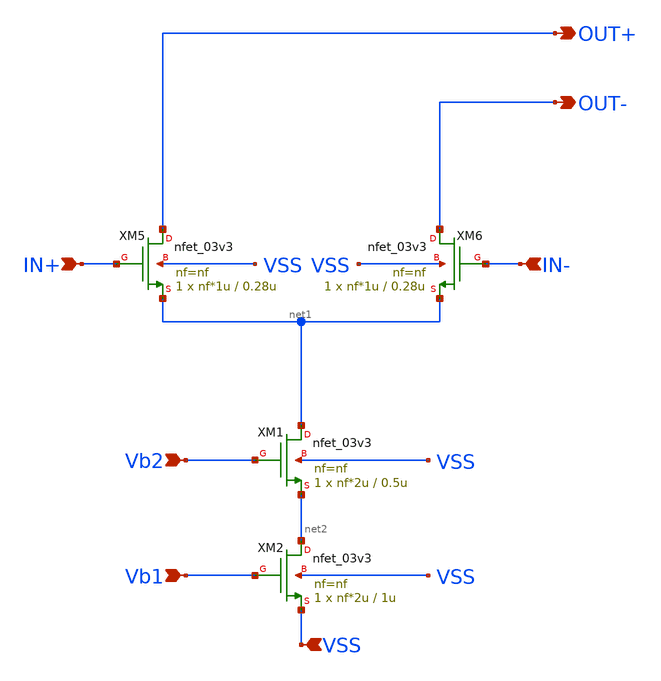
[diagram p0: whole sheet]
** sch_path: DAC/xschem/dac_current_unit.sch
**.subckt dac_current_unit IN+ IN- OUT- OUT+ Vb2 Vb1 VSS
*.ipin IN+
*.ipin IN-
*.opin OUT-
*.opin OUT+
*.ipin Vb2
*.ipin Vb1
*.ipin VSS
XM1 net1 Vb2 net2 VSS nfet_03v3 L=0.5u W=nf*2u nf=nf ad='int((nf+1)/2) * W/nf * 0.18u' as='int((nf+2)/2) * W/nf * 0.18u'
+ pd='2*int((nf+1)/2) * (W/nf + 0.18u)' ps='2*int((nf+2)/2) * (W/nf + 0.18u)' nrd='0.18u / W' nrs='0.18u / W'
+ sa=0 sb=0 sd=0 m=1
XM2 net2 Vb1 VSS VSS nfet_03v3 L=1u W=nf*2u nf=nf ad='int((nf+1)/2) * W/nf * 0.18u' as='int((nf+2)/2) * W/nf * 0.18u'
+ pd='2*int((nf+1)/2) * (W/nf + 0.18u)' ps='2*int((nf+2)/2) * (W/nf + 0.18u)' nrd='0.18u / W' nrs='0.18u / W'
+ sa=0 sb=0 sd=0 m=1
XM5 OUT+ IN+ net1 VSS nfet_03v3 L=0.28u W=nf*1u nf=nf ad='int((nf+1)/2) * W/nf * 0.18u' as='int((nf+2)/2) * W/nf * 0.18u'
+ pd='2*int((nf+1)/2) * (W/nf + 0.18u)' ps='2*int((nf+2)/2) * (W/nf + 0.18u)' nrd='0.18u / W' nrs='0.18u / W'
+ sa=0 sb=0 sd=0 m=1
XM6 OUT- IN- net1 VSS nfet_03v3 L=0.28u W=nf*1u nf=nf ad='int((nf+1)/2) * W/nf * 0.18u' as='int((nf+2)/2) * W/nf * 0.18u'
+ pd='2*int((nf+1)/2) * (W/nf + 0.18u)' ps='2*int((nf+2)/2) * (W/nf + 0.18u)' nrd='0.18u / W' nrs='0.18u / W'
+ sa=0 sb=0 sd=0 m=1
**.ends
.end
